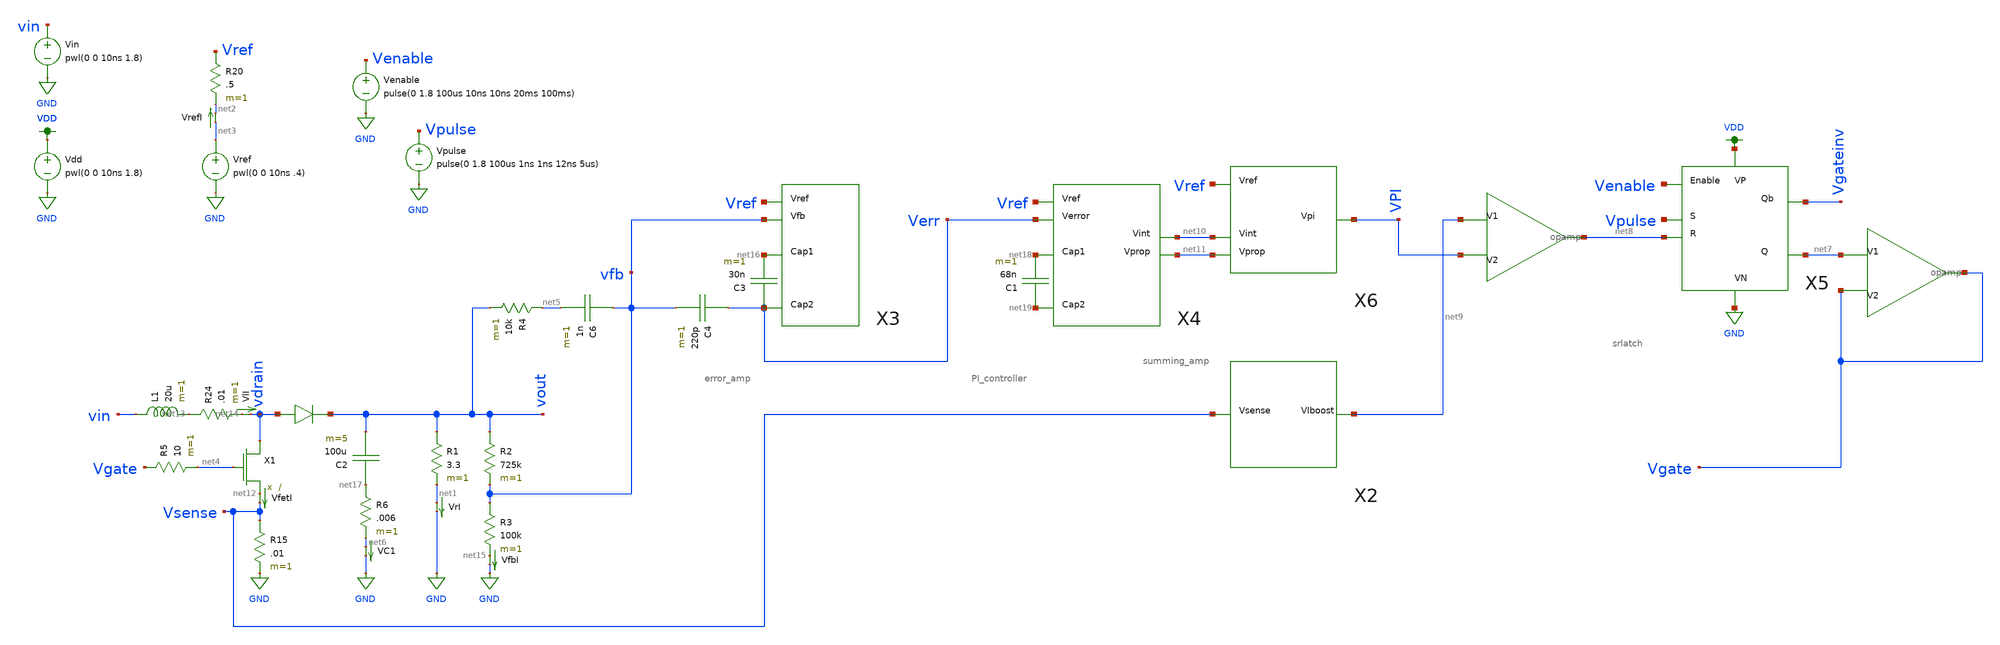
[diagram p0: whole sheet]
** sch_path: schematics/old/boost_CMC_tmp.sch
**.subckt boost_CMC_tmp
Vin vin GND pwl(0 0 10ns 1.8)
VfetI net12 Vsense 0
.save i(vfeti)
X1 vdrain net4 net12 power_nfet
L1 vin net13 20u m=1
D1 vdrain vout diode_schottky
R1 vout net1 3.3 m=1
VlI net14 vdrain 0
.save i(vli)
VrI net1 GND 0
.save i(vri)
R2 vout vfb 725k m=1
R3 vfb net15 100k m=1
Vdd VDD GND pwl(0 0 10ns 1.8)
Vref net3 GND pwl(0 0 10ns .4)
X11 net9 VPI net8 opamp
Vpulse Vpulse GND pulse(0 1.8 100us 1ns 1ns 12ns 5us)
VrefI net3 net2 0
.save i(vrefi)
R24 net13 net14 .01 m=1
VfbI net15 GND 0
.save i(vfbi)
R20 Vref net2 .5 m=1
C3 Verr net16 30n m=1
C4 Verr vfb 220p m=1
R4 net5 vout 10k m=1
C6 vfb net5 1n m=1
R5 Vgate net4 10 m=1
C2 net17 vout 100u m=5
R6 net17 net6 .006 m=1
VC1 net6 GND 0
.save i(vc1)
R15 Vsense GND .01 m=1
X5 Venable Vpulse net8 VDD GND Vgateinv net7 srlatch
X10 net7 Vgate Vgate opamp
Venable Venable GND pulse(0 1.8 100us 10ns 10ns 20ms 100ms)
X2 Vsense net9 current_boost
X3 Vref net16 vfb Verr error_amp
X4 Vref net18 Verr net19 net10 net11 PI_controller
C1 net19 net18 68n m=1
X6 Vref VPI net10 net11 summing_amp
**** begin user architecture code


.include ~/Documents/MADVLSI_final/schematics/models/power_nfet_model.spice
.include ~/Documents/MADVLSI_final/schematics/models/diode_schottky_model.spice
.options gmin=1e-10
.options abstol=1e-10
.options reltol=.003
.tran 100ns 10ms
.save v(vout)


.option wnflag=1
.lib ~/skywater/skywater-pdk/libraries/sky130_fd_pr_ngspice/latest/models/sky130.lib.spice tt

**** end user architecture code
**.ends

* expanding   symbol:  /home/madvlsi/Documents/MADVLSI_final/schematics/opamp.sym # of pins=3
** sym_path: schematics/opamp.sym
** sch_path: schematics/opamp.sch
.subckt opamp V1 V2 VOUT
*.ipin V1
*.ipin V2
*.opin VOUT
XM19 net12 net10 GND VDD sky130_fd_pr__pfet_01v8 L=.6 W=1.5 nf=1 ad='int((nf+1)/2) * W/nf * 0.29' as='int((nf+2)/2) * W/nf * 0.29'
+ pd='2*int((nf+1)/2) * (W/nf + 0.29)' ps='2*int((nf+2)/2) * (W/nf + 0.29)' nrd='0.29 / W' nrs='0.29 / W'
+ sa=0 sb=0 sd=0 mult=1 m=1
XMD20 VDD VDD net12 VDD sky130_fd_pr__pfet_01v8 L=.6 W=1.5 nf=1 ad='int((nf+1)/2) * W/nf * 0.29' as='int((nf+2)/2) * W/nf * 0.29'
+ pd='2*int((nf+1)/2) * (W/nf + 0.29)' ps='2*int((nf+2)/2) * (W/nf + 0.29)' nrd='0.29 / W' nrs='0.29 / W'
+ sa=0 sb=0 sd=0 mult=1 m=1
XM22 net12 net10 net9 VDD sky130_fd_pr__pfet_01v8 L=.6 W=1.5 nf=1 ad='int((nf+1)/2) * W/nf * 0.29' as='int((nf+2)/2) * W/nf * 0.29'
+ pd='2*int((nf+1)/2) * (W/nf + 0.29)' ps='2*int((nf+2)/2) * (W/nf + 0.29)' nrd='0.29 / W' nrs='0.29 / W'
+ sa=0 sb=0 sd=0 mult=1 m=1
XM23 GND net10 net12 VDD sky130_fd_pr__pfet_01v8 L=.6 W=1.5 nf=1 ad='int((nf+1)/2) * W/nf * 0.29' as='int((nf+2)/2) * W/nf * 0.29'
+ pd='2*int((nf+1)/2) * (W/nf + 0.29)' ps='2*int((nf+2)/2) * (W/nf + 0.29)' nrd='0.29 / W' nrs='0.29 / W'
+ sa=0 sb=0 sd=0 mult=1 m=1
XMD24 net9 VDD net10 VDD sky130_fd_pr__pfet_01v8 L=.6 W=1.5 nf=1 ad='int((nf+1)/2) * W/nf * 0.29' as='int((nf+2)/2) * W/nf * 0.29'
+ pd='2*int((nf+1)/2) * (W/nf + 0.29)' ps='2*int((nf+2)/2) * (W/nf + 0.29)' nrd='0.29 / W' nrs='0.29 / W'
+ sa=0 sb=0 sd=0 mult=1 m=1
XM25 VDD net10 net12 VDD sky130_fd_pr__pfet_01v8 L=.6 W=1.5 nf=1 ad='int((nf+1)/2) * W/nf * 0.29' as='int((nf+2)/2) * W/nf * 0.29'
+ pd='2*int((nf+1)/2) * (W/nf + 0.29)' ps='2*int((nf+2)/2) * (W/nf + 0.29)' nrd='0.29 / W' nrs='0.29 / W'
+ sa=0 sb=0 sd=0 mult=1 m=1
XM26 net7 V2 net11 VDD sky130_fd_pr__pfet_01v8 L=.6 W=1.5 nf=1 ad='int((nf+1)/2) * W/nf * 0.29' as='int((nf+2)/2) * W/nf * 0.29'
+ pd='2*int((nf+1)/2) * (W/nf + 0.29)' ps='2*int((nf+2)/2) * (W/nf + 0.29)' nrd='0.29 / W' nrs='0.29 / W'
+ sa=0 sb=0 sd=0 mult=1 m=1
XMD27 net5 VDD net14 VDD sky130_fd_pr__pfet_01v8 L=.6 W=1.5 nf=1 ad='int((nf+1)/2) * W/nf * 0.29' as='int((nf+2)/2) * W/nf * 0.29'
+ pd='2*int((nf+1)/2) * (W/nf + 0.29)' ps='2*int((nf+2)/2) * (W/nf + 0.29)' nrd='0.29 / W' nrs='0.29 / W'
+ sa=0 sb=0 sd=0 mult=1 m=1
XM28 net6 V1 net11 VDD sky130_fd_pr__pfet_01v8 L=.6 W=1.5 nf=1 ad='int((nf+1)/2) * W/nf * 0.29' as='int((nf+2)/2) * W/nf * 0.29'
+ pd='2*int((nf+1)/2) * (W/nf + 0.29)' ps='2*int((nf+2)/2) * (W/nf + 0.29)' nrd='0.29 / W' nrs='0.29 / W'
+ sa=0 sb=0 sd=0 mult=1 m=1
XM29 net11 net10 VDD VDD sky130_fd_pr__pfet_01v8 L=.6 W=1.5 nf=1 ad='int((nf+1)/2) * W/nf * 0.29' as='int((nf+2)/2) * W/nf * 0.29'
+ pd='2*int((nf+1)/2) * (W/nf + 0.29)' ps='2*int((nf+2)/2) * (W/nf + 0.29)' nrd='0.29 / W' nrs='0.29 / W'
+ sa=0 sb=0 sd=0 mult=1 m=1
XMD30 net11 VDD VDD VDD sky130_fd_pr__pfet_01v8 L=.6 W=1.5 nf=1 ad='int((nf+1)/2) * W/nf * 0.29' as='int((nf+2)/2) * W/nf * 0.29'
+ pd='2*int((nf+1)/2) * (W/nf + 0.29)' ps='2*int((nf+2)/2) * (W/nf + 0.29)' nrd='0.29 / W' nrs='0.29 / W'
+ sa=0 sb=0 sd=0 mult=1 m=1
XMD31 net2 VDD net13 VDD sky130_fd_pr__pfet_01v8 L=.6 W=1.5 nf=1 ad='int((nf+1)/2) * W/nf * 0.29' as='int((nf+2)/2) * W/nf * 0.29'
+ pd='2*int((nf+1)/2) * (W/nf + 0.29)' ps='2*int((nf+2)/2) * (W/nf + 0.29)' nrd='0.29 / W' nrs='0.29 / W'
+ sa=0 sb=0 sd=0 mult=1 m=1
XM32 net4 net5 net5 VDD sky130_fd_pr__pfet_01v8 L=.6 W=1.5 nf=1 ad='int((nf+1)/2) * W/nf * 0.29' as='int((nf+2)/2) * W/nf * 0.29'
+ pd='2*int((nf+1)/2) * (W/nf + 0.29)' ps='2*int((nf+2)/2) * (W/nf + 0.29)' nrd='0.29 / W' nrs='0.29 / W'
+ sa=0 sb=0 sd=0 mult=1 m=1
XM33 VDD net10 net4 VDD sky130_fd_pr__pfet_01v8 L=.6 W=1.5 nf=1 ad='int((nf+1)/2) * W/nf * 0.29' as='int((nf+2)/2) * W/nf * 0.29'
+ pd='2*int((nf+1)/2) * (W/nf + 0.29)' ps='2*int((nf+2)/2) * (W/nf + 0.29)' nrd='0.29 / W' nrs='0.29 / W'
+ sa=0 sb=0 sd=0 mult=1 m=1
XM34 net3 net5 net2 VDD sky130_fd_pr__pfet_01v8 L=.6 W=1.5 nf=1 ad='int((nf+1)/2) * W/nf * 0.29' as='int((nf+2)/2) * W/nf * 0.29'
+ pd='2*int((nf+1)/2) * (W/nf + 0.29)' ps='2*int((nf+2)/2) * (W/nf + 0.29)' nrd='0.29 / W' nrs='0.29 / W'
+ sa=0 sb=0 sd=0 mult=1 m=1
XM35 VDD net10 net3 VDD sky130_fd_pr__pfet_01v8 L=.6 W=1.5 nf=1 ad='int((nf+1)/2) * W/nf * 0.29' as='int((nf+2)/2) * W/nf * 0.29'
+ pd='2*int((nf+1)/2) * (W/nf + 0.29)' ps='2*int((nf+2)/2) * (W/nf + 0.29)' nrd='0.29 / W' nrs='0.29 / W'
+ sa=0 sb=0 sd=0 mult=1 m=1
XM36 VOUT net2 VDD VDD sky130_fd_pr__pfet_01v8 L=.6 W=1.5 nf=1 ad='int((nf+1)/2) * W/nf * 0.29' as='int((nf+2)/2) * W/nf * 0.29'
+ pd='2*int((nf+1)/2) * (W/nf + 0.29)' ps='2*int((nf+2)/2) * (W/nf + 0.29)' nrd='0.29 / W' nrs='0.29 / W'
+ sa=0 sb=0 sd=0 mult=1 m=1
XM37 VDD net2 VOUT VDD sky130_fd_pr__pfet_01v8 L=.6 W=1.5 nf=1 ad='int((nf+1)/2) * W/nf * 0.29' as='int((nf+2)/2) * W/nf * 0.29'
+ pd='2*int((nf+1)/2) * (W/nf + 0.29)' ps='2*int((nf+2)/2) * (W/nf + 0.29)' nrd='0.29 / W' nrs='0.29 / W'
+ sa=0 sb=0 sd=0 mult=1 m=1
XM38 VOUT net2 VDD VDD sky130_fd_pr__pfet_01v8 L=.6 W=1.5 nf=1 ad='int((nf+1)/2) * W/nf * 0.29' as='int((nf+2)/2) * W/nf * 0.29'
+ pd='2*int((nf+1)/2) * (W/nf + 0.29)' ps='2*int((nf+2)/2) * (W/nf + 0.29)' nrd='0.29 / W' nrs='0.29 / W'
+ sa=0 sb=0 sd=0 mult=1 m=1
XM39 VDD net2 VOUT VDD sky130_fd_pr__pfet_01v8 L=.6 W=1.5 nf=1 ad='int((nf+1)/2) * W/nf * 0.29' as='int((nf+2)/2) * W/nf * 0.29'
+ pd='2*int((nf+1)/2) * (W/nf + 0.29)' ps='2*int((nf+2)/2) * (W/nf + 0.29)' nrd='0.29 / W' nrs='0.29 / W'
+ sa=0 sb=0 sd=0 mult=1 m=1
XM40 net1 net9 VDD GND sky130_fd_pr__nfet_01v8 L=.6 W=1.5 nf=1 ad='int((nf+1)/2) * W/nf * 0.29' as='int((nf+2)/2) * W/nf * 0.29'
+ pd='2*int((nf+1)/2) * (W/nf + 0.29)' ps='2*int((nf+2)/2) * (W/nf + 0.29)' nrd='0.29 / W' nrs='0.29 / W'
+ sa=0 sb=0 sd=0 mult=1 m=1
XMD41 GND GND net1 GND sky130_fd_pr__nfet_01v8 L=.6 W=1.5 nf=1 ad='int((nf+1)/2) * W/nf * 0.29' as='int((nf+2)/2) * W/nf * 0.29'
+ pd='2*int((nf+1)/2) * (W/nf + 0.29)' ps='2*int((nf+2)/2) * (W/nf + 0.29)' nrd='0.29 / W' nrs='0.29 / W'
+ sa=0 sb=0 sd=0 mult=1 m=1
XM42 net1 net9 net10 GND sky130_fd_pr__nfet_01v8 L=.6 W=1.5 nf=1 ad='int((nf+1)/2) * W/nf * 0.29' as='int((nf+2)/2) * W/nf * 0.29'
+ pd='2*int((nf+1)/2) * (W/nf + 0.29)' ps='2*int((nf+2)/2) * (W/nf + 0.29)' nrd='0.29 / W' nrs='0.29 / W'
+ sa=0 sb=0 sd=0 mult=1 m=1
XM43 VDD net9 net1 GND sky130_fd_pr__nfet_01v8 L=.6 W=1.5 nf=1 ad='int((nf+1)/2) * W/nf * 0.29' as='int((nf+2)/2) * W/nf * 0.29'
+ pd='2*int((nf+1)/2) * (W/nf + 0.29)' ps='2*int((nf+2)/2) * (W/nf + 0.29)' nrd='0.29 / W' nrs='0.29 / W'
+ sa=0 sb=0 sd=0 mult=1 m=1
XMD44 net10 GND net9 GND sky130_fd_pr__nfet_01v8 L=.6 W=1.5 nf=1 ad='int((nf+1)/2) * W/nf * 0.29' as='int((nf+2)/2) * W/nf * 0.29'
+ pd='2*int((nf+1)/2) * (W/nf + 0.29)' ps='2*int((nf+2)/2) * (W/nf + 0.29)' nrd='0.29 / W' nrs='0.29 / W'
+ sa=0 sb=0 sd=0 mult=1 m=1
XM45 GND net9 net1 GND sky130_fd_pr__nfet_01v8 L=.6 W=1.5 nf=1 ad='int((nf+1)/2) * W/nf * 0.29' as='int((nf+2)/2) * W/nf * 0.29'
+ pd='2*int((nf+1)/2) * (W/nf + 0.29)' ps='2*int((nf+2)/2) * (W/nf + 0.29)' nrd='0.29 / W' nrs='0.29 / W'
+ sa=0 sb=0 sd=0 mult=1 m=1
XM46 net3 V1 net8 GND sky130_fd_pr__nfet_01v8 L=.6 W=1.5 nf=1 ad='int((nf+1)/2) * W/nf * 0.29' as='int((nf+2)/2) * W/nf * 0.29'
+ pd='2*int((nf+1)/2) * (W/nf + 0.29)' ps='2*int((nf+2)/2) * (W/nf + 0.29)' nrd='0.29 / W' nrs='0.29 / W'
+ sa=0 sb=0 sd=0 mult=1 m=1
XMD47 net5 GND net15 GND sky130_fd_pr__nfet_01v8 L=.6 W=1.5 nf=1 ad='int((nf+1)/2) * W/nf * 0.29' as='int((nf+2)/2) * W/nf * 0.29'
+ pd='2*int((nf+1)/2) * (W/nf + 0.29)' ps='2*int((nf+2)/2) * (W/nf + 0.29)' nrd='0.29 / W' nrs='0.29 / W'
+ sa=0 sb=0 sd=0 mult=1 m=1
XM48 net4 V2 net8 GND sky130_fd_pr__nfet_01v8 L=.6 W=1.5 nf=1 ad='int((nf+1)/2) * W/nf * 0.29' as='int((nf+2)/2) * W/nf * 0.29'
+ pd='2*int((nf+1)/2) * (W/nf + 0.29)' ps='2*int((nf+2)/2) * (W/nf + 0.29)' nrd='0.29 / W' nrs='0.29 / W'
+ sa=0 sb=0 sd=0 mult=1 m=1
XM49 net8 net9 GND GND sky130_fd_pr__nfet_01v8 L=.6 W=1.5 nf=1 ad='int((nf+1)/2) * W/nf * 0.29' as='int((nf+2)/2) * W/nf * 0.29'
+ pd='2*int((nf+1)/2) * (W/nf + 0.29)' ps='2*int((nf+2)/2) * (W/nf + 0.29)' nrd='0.29 / W' nrs='0.29 / W'
+ sa=0 sb=0 sd=0 mult=1 m=1
XMD50 net8 GND GND GND sky130_fd_pr__nfet_01v8 L=.6 W=1.5 nf=1 ad='int((nf+1)/2) * W/nf * 0.29' as='int((nf+2)/2) * W/nf * 0.29'
+ pd='2*int((nf+1)/2) * (W/nf + 0.29)' ps='2*int((nf+2)/2) * (W/nf + 0.29)' nrd='0.29 / W' nrs='0.29 / W'
+ sa=0 sb=0 sd=0 mult=1 m=1
XMD51 net2 GND net16 GND sky130_fd_pr__nfet_01v8 L=.6 W=1.5 nf=1 ad='int((nf+1)/2) * W/nf * 0.29' as='int((nf+2)/2) * W/nf * 0.29'
+ pd='2*int((nf+1)/2) * (W/nf + 0.29)' ps='2*int((nf+2)/2) * (W/nf + 0.29)' nrd='0.29 / W' nrs='0.29 / W'
+ sa=0 sb=0 sd=0 mult=1 m=1
XM52 GND net9 net7 GND sky130_fd_pr__nfet_01v8 L=.6 W=1.5 nf=1 ad='int((nf+1)/2) * W/nf * 0.29' as='int((nf+2)/2) * W/nf * 0.29'
+ pd='2*int((nf+1)/2) * (W/nf + 0.29)' ps='2*int((nf+2)/2) * (W/nf + 0.29)' nrd='0.29 / W' nrs='0.29 / W'
+ sa=0 sb=0 sd=0 mult=1 m=1
XMD53 VOUT GND GND GND sky130_fd_pr__nfet_01v8 L=.6 W=1.5 nf=1 ad='int((nf+1)/2) * W/nf * 0.29' as='int((nf+2)/2) * W/nf * 0.29'
+ pd='2*int((nf+1)/2) * (W/nf + 0.29)' ps='2*int((nf+2)/2) * (W/nf + 0.29)' nrd='0.29 / W' nrs='0.29 / W'
+ sa=0 sb=0 sd=0 mult=1 m=1
XM54 GND net9 net6 GND sky130_fd_pr__nfet_01v8 L=.6 W=1.5 nf=1 ad='int((nf+1)/2) * W/nf * 0.29' as='int((nf+2)/2) * W/nf * 0.29'
+ pd='2*int((nf+1)/2) * (W/nf + 0.29)' ps='2*int((nf+2)/2) * (W/nf + 0.29)' nrd='0.29 / W' nrs='0.29 / W'
+ sa=0 sb=0 sd=0 mult=1 m=1
XM55 net7 net5 net5 GND sky130_fd_pr__nfet_01v8 L=.6 W=1.5 nf=1 ad='int((nf+1)/2) * W/nf * 0.29' as='int((nf+2)/2) * W/nf * 0.29'
+ pd='2*int((nf+1)/2) * (W/nf + 0.29)' ps='2*int((nf+2)/2) * (W/nf + 0.29)' nrd='0.29 / W' nrs='0.29 / W'
+ sa=0 sb=0 sd=0 mult=1 m=1
XM56 net6 net5 net2 GND sky130_fd_pr__nfet_01v8 L=.6 W=1.5 nf=1 ad='int((nf+1)/2) * W/nf * 0.29' as='int((nf+2)/2) * W/nf * 0.29'
+ pd='2*int((nf+1)/2) * (W/nf + 0.29)' ps='2*int((nf+2)/2) * (W/nf + 0.29)' nrd='0.29 / W' nrs='0.29 / W'
+ sa=0 sb=0 sd=0 mult=1 m=1
XMD57 VOUT GND GND GND sky130_fd_pr__nfet_01v8 L=.6 W=1.5 nf=1 ad='int((nf+1)/2) * W/nf * 0.29' as='int((nf+2)/2) * W/nf * 0.29'
+ pd='2*int((nf+1)/2) * (W/nf + 0.29)' ps='2*int((nf+2)/2) * (W/nf + 0.29)' nrd='0.29 / W' nrs='0.29 / W'
+ sa=0 sb=0 sd=0 mult=1 m=1
XM58 GND net2 VOUT GND sky130_fd_pr__nfet_01v8 L=.6 W=1.5 nf=1 ad='int((nf+1)/2) * W/nf * 0.29' as='int((nf+2)/2) * W/nf * 0.29'
+ pd='2*int((nf+1)/2) * (W/nf + 0.29)' ps='2*int((nf+2)/2) * (W/nf + 0.29)' nrd='0.29 / W' nrs='0.29 / W'
+ sa=0 sb=0 sd=0 mult=1 m=1
XM59 GND net2 VOUT GND sky130_fd_pr__nfet_01v8 L=.6 W=1.5 nf=1 ad='int((nf+1)/2) * W/nf * 0.29' as='int((nf+2)/2) * W/nf * 0.29'
+ pd='2*int((nf+1)/2) * (W/nf + 0.29)' ps='2*int((nf+2)/2) * (W/nf + 0.29)' nrd='0.29 / W' nrs='0.29 / W'
+ sa=0 sb=0 sd=0 mult=1 m=1
XM60 net12 net10 GND VDD sky130_fd_pr__pfet_01v8 L=.6 W=1.5 nf=1 ad='int((nf+1)/2) * W/nf * 0.29' as='int((nf+2)/2) * W/nf * 0.29'
+ pd='2*int((nf+1)/2) * (W/nf + 0.29)' ps='2*int((nf+2)/2) * (W/nf + 0.29)' nrd='0.29 / W' nrs='0.29 / W'
+ sa=0 sb=0 sd=0 mult=1 m=1
XM61 net10 net10 net4 VDD sky130_fd_pr__pfet_01v8 L=.6 W=1.5 nf=1 ad='int((nf+1)/2) * W/nf * 0.29' as='int((nf+2)/2) * W/nf * 0.29'
+ pd='2*int((nf+1)/2) * (W/nf + 0.29)' ps='2*int((nf+2)/2) * (W/nf + 0.29)' nrd='0.29 / W' nrs='0.29 / W'
+ sa=0 sb=0 sd=0 mult=1 m=1
XM62 net1 net9 VDD GND sky130_fd_pr__nfet_01v8 L=.6 W=1.5 nf=1 ad='int((nf+1)/2) * W/nf * 0.29' as='int((nf+2)/2) * W/nf * 0.29'
+ pd='2*int((nf+1)/2) * (W/nf + 0.29)' ps='2*int((nf+2)/2) * (W/nf + 0.29)' nrd='0.29 / W' nrs='0.29 / W'
+ sa=0 sb=0 sd=0 mult=1 m=1
XM63 net9 net9 net7 GND sky130_fd_pr__nfet_01v8 L=.6 W=1.5 nf=1 ad='int((nf+1)/2) * W/nf * 0.29' as='int((nf+2)/2) * W/nf * 0.29'
+ pd='2*int((nf+1)/2) * (W/nf + 0.29)' ps='2*int((nf+2)/2) * (W/nf + 0.29)' nrd='0.29 / W' nrs='0.29 / W'
+ sa=0 sb=0 sd=0 mult=1 m=1
XMD64 VDD GND GND GND sky130_fd_pr__nfet_01v8 L=.6 W=1.5 nf=1 ad='int((nf+1)/2) * W/nf * 0.29' as='int((nf+2)/2) * W/nf * 0.29'
+ pd='2*int((nf+1)/2) * (W/nf + 0.29)' ps='2*int((nf+2)/2) * (W/nf + 0.29)' nrd='0.29 / W' nrs='0.29 / W'
+ sa=0 sb=0 sd=0 mult=1 m=1
XMD65 net7 GND GND GND sky130_fd_pr__nfet_01v8 L=.6 W=1.5 nf=1 ad='int((nf+1)/2) * W/nf * 0.29' as='int((nf+2)/2) * W/nf * 0.29'
+ pd='2*int((nf+1)/2) * (W/nf + 0.29)' ps='2*int((nf+2)/2) * (W/nf + 0.29)' nrd='0.29 / W' nrs='0.29 / W'
+ sa=0 sb=0 sd=0 mult=1 m=1
XMD66 GND VDD VDD VDD sky130_fd_pr__pfet_01v8 L=.6 W=1.5 nf=1 ad='int((nf+1)/2) * W/nf * 0.29' as='int((nf+2)/2) * W/nf * 0.29'
+ pd='2*int((nf+1)/2) * (W/nf + 0.29)' ps='2*int((nf+2)/2) * (W/nf + 0.29)' nrd='0.29 / W' nrs='0.29 / W'
+ sa=0 sb=0 sd=0 mult=1 m=1
XMD67 net4 VDD VDD VDD sky130_fd_pr__pfet_01v8 L=.6 W=1.5 nf=1 ad='int((nf+1)/2) * W/nf * 0.29' as='int((nf+2)/2) * W/nf * 0.29'
+ pd='2*int((nf+1)/2) * (W/nf + 0.29)' ps='2*int((nf+2)/2) * (W/nf + 0.29)' nrd='0.29 / W' nrs='0.29 / W'
+ sa=0 sb=0 sd=0 mult=1 m=1
XMD1 net15 GND net3 GND sky130_fd_pr__nfet_01v8 L=.6 W=1.5 nf=1 ad='int((nf+1)/2) * W/nf * 0.29' as='int((nf+2)/2) * W/nf * 0.29'
+ pd='2*int((nf+1)/2) * (W/nf + 0.29)' ps='2*int((nf+2)/2) * (W/nf + 0.29)' nrd='0.29 / W' nrs='0.29 / W'
+ sa=0 sb=0 sd=0 mult=1 m=1
XMD2 net16 GND net4 GND sky130_fd_pr__nfet_01v8 L=.6 W=1.5 nf=1 ad='int((nf+1)/2) * W/nf * 0.29' as='int((nf+2)/2) * W/nf * 0.29'
+ pd='2*int((nf+1)/2) * (W/nf + 0.29)' ps='2*int((nf+2)/2) * (W/nf + 0.29)' nrd='0.29 / W' nrs='0.29 / W'
+ sa=0 sb=0 sd=0 mult=1 m=1
XMD3 net13 VDD net6 VDD sky130_fd_pr__pfet_01v8 L=.6 W=1.5 nf=1 ad='int((nf+1)/2) * W/nf * 0.29' as='int((nf+2)/2) * W/nf * 0.29'
+ pd='2*int((nf+1)/2) * (W/nf + 0.29)' ps='2*int((nf+2)/2) * (W/nf + 0.29)' nrd='0.29 / W' nrs='0.29 / W'
+ sa=0 sb=0 sd=0 mult=1 m=1
XMD4 net14 VDD net7 VDD sky130_fd_pr__pfet_01v8 L=.6 W=1.5 nf=1 ad='int((nf+1)/2) * W/nf * 0.29' as='int((nf+2)/2) * W/nf * 0.29'
+ pd='2*int((nf+1)/2) * (W/nf + 0.29)' ps='2*int((nf+2)/2) * (W/nf + 0.29)' nrd='0.29 / W' nrs='0.29 / W'
+ sa=0 sb=0 sd=0 mult=1 m=1
XM1 net21 net10 GND VDD sky130_fd_pr__pfet_01v8 L=.6 W=1.5 nf=1 ad='int((nf+1)/2) * W/nf * 0.29' as='int((nf+2)/2) * W/nf * 0.29'
+ pd='2*int((nf+1)/2) * (W/nf + 0.29)' ps='2*int((nf+2)/2) * (W/nf + 0.29)' nrd='0.29 / W' nrs='0.29 / W'
+ sa=0 sb=0 sd=0 mult=1 m=1
XMD5 VDD VDD net21 VDD sky130_fd_pr__pfet_01v8 L=.6 W=1.5 nf=1 ad='int((nf+1)/2) * W/nf * 0.29' as='int((nf+2)/2) * W/nf * 0.29'
+ pd='2*int((nf+1)/2) * (W/nf + 0.29)' ps='2*int((nf+2)/2) * (W/nf + 0.29)' nrd='0.29 / W' nrs='0.29 / W'
+ sa=0 sb=0 sd=0 mult=1 m=1
XM6 net21 net10 net9 VDD sky130_fd_pr__pfet_01v8 L=.6 W=1.5 nf=1 ad='int((nf+1)/2) * W/nf * 0.29' as='int((nf+2)/2) * W/nf * 0.29'
+ pd='2*int((nf+1)/2) * (W/nf + 0.29)' ps='2*int((nf+2)/2) * (W/nf + 0.29)' nrd='0.29 / W' nrs='0.29 / W'
+ sa=0 sb=0 sd=0 mult=1 m=1
XM7 GND net10 net21 VDD sky130_fd_pr__pfet_01v8 L=.6 W=1.5 nf=1 ad='int((nf+1)/2) * W/nf * 0.29' as='int((nf+2)/2) * W/nf * 0.29'
+ pd='2*int((nf+1)/2) * (W/nf + 0.29)' ps='2*int((nf+2)/2) * (W/nf + 0.29)' nrd='0.29 / W' nrs='0.29 / W'
+ sa=0 sb=0 sd=0 mult=1 m=1
XMD8 net9 VDD net10 VDD sky130_fd_pr__pfet_01v8 L=.6 W=1.5 nf=1 ad='int((nf+1)/2) * W/nf * 0.29' as='int((nf+2)/2) * W/nf * 0.29'
+ pd='2*int((nf+1)/2) * (W/nf + 0.29)' ps='2*int((nf+2)/2) * (W/nf + 0.29)' nrd='0.29 / W' nrs='0.29 / W'
+ sa=0 sb=0 sd=0 mult=1 m=1
XM9 VDD net10 net21 VDD sky130_fd_pr__pfet_01v8 L=.6 W=1.5 nf=1 ad='int((nf+1)/2) * W/nf * 0.29' as='int((nf+2)/2) * W/nf * 0.29'
+ pd='2*int((nf+1)/2) * (W/nf + 0.29)' ps='2*int((nf+2)/2) * (W/nf + 0.29)' nrd='0.29 / W' nrs='0.29 / W'
+ sa=0 sb=0 sd=0 mult=1 m=1
XM10 net7 V2 net20 VDD sky130_fd_pr__pfet_01v8 L=.6 W=1.5 nf=1 ad='int((nf+1)/2) * W/nf * 0.29' as='int((nf+2)/2) * W/nf * 0.29'
+ pd='2*int((nf+1)/2) * (W/nf + 0.29)' ps='2*int((nf+2)/2) * (W/nf + 0.29)' nrd='0.29 / W' nrs='0.29 / W'
+ sa=0 sb=0 sd=0 mult=1 m=1
XMD11 net18 VDD net23 VDD sky130_fd_pr__pfet_01v8 L=.6 W=1.5 nf=1 ad='int((nf+1)/2) * W/nf * 0.29' as='int((nf+2)/2) * W/nf * 0.29'
+ pd='2*int((nf+1)/2) * (W/nf + 0.29)' ps='2*int((nf+2)/2) * (W/nf + 0.29)' nrd='0.29 / W' nrs='0.29 / W'
+ sa=0 sb=0 sd=0 mult=1 m=1
XM12 net6 V1 net20 VDD sky130_fd_pr__pfet_01v8 L=.6 W=1.5 nf=1 ad='int((nf+1)/2) * W/nf * 0.29' as='int((nf+2)/2) * W/nf * 0.29'
+ pd='2*int((nf+1)/2) * (W/nf + 0.29)' ps='2*int((nf+2)/2) * (W/nf + 0.29)' nrd='0.29 / W' nrs='0.29 / W'
+ sa=0 sb=0 sd=0 mult=1 m=1
XM13 net20 net10 VDD VDD sky130_fd_pr__pfet_01v8 L=.6 W=1.5 nf=1 ad='int((nf+1)/2) * W/nf * 0.29' as='int((nf+2)/2) * W/nf * 0.29'
+ pd='2*int((nf+1)/2) * (W/nf + 0.29)' ps='2*int((nf+2)/2) * (W/nf + 0.29)' nrd='0.29 / W' nrs='0.29 / W'
+ sa=0 sb=0 sd=0 mult=1 m=1
XMD14 net20 VDD VDD VDD sky130_fd_pr__pfet_01v8 L=.6 W=1.5 nf=1 ad='int((nf+1)/2) * W/nf * 0.29' as='int((nf+2)/2) * W/nf * 0.29'
+ pd='2*int((nf+1)/2) * (W/nf + 0.29)' ps='2*int((nf+2)/2) * (W/nf + 0.29)' nrd='0.29 / W' nrs='0.29 / W'
+ sa=0 sb=0 sd=0 mult=1 m=1
XMD15 net2 VDD net22 VDD sky130_fd_pr__pfet_01v8 L=.6 W=1.5 nf=1 ad='int((nf+1)/2) * W/nf * 0.29' as='int((nf+2)/2) * W/nf * 0.29'
+ pd='2*int((nf+1)/2) * (W/nf + 0.29)' ps='2*int((nf+2)/2) * (W/nf + 0.29)' nrd='0.29 / W' nrs='0.29 / W'
+ sa=0 sb=0 sd=0 mult=1 m=1
XM16 net4 net18 net18 VDD sky130_fd_pr__pfet_01v8 L=.6 W=1.5 nf=1 ad='int((nf+1)/2) * W/nf * 0.29' as='int((nf+2)/2) * W/nf * 0.29'
+ pd='2*int((nf+1)/2) * (W/nf + 0.29)' ps='2*int((nf+2)/2) * (W/nf + 0.29)' nrd='0.29 / W' nrs='0.29 / W'
+ sa=0 sb=0 sd=0 mult=1 m=1
XM17 VDD net10 net4 VDD sky130_fd_pr__pfet_01v8 L=.6 W=1.5 nf=1 ad='int((nf+1)/2) * W/nf * 0.29' as='int((nf+2)/2) * W/nf * 0.29'
+ pd='2*int((nf+1)/2) * (W/nf + 0.29)' ps='2*int((nf+2)/2) * (W/nf + 0.29)' nrd='0.29 / W' nrs='0.29 / W'
+ sa=0 sb=0 sd=0 mult=1 m=1
XM18 net3 net18 net2 VDD sky130_fd_pr__pfet_01v8 L=.6 W=1.5 nf=1 ad='int((nf+1)/2) * W/nf * 0.29' as='int((nf+2)/2) * W/nf * 0.29'
+ pd='2*int((nf+1)/2) * (W/nf + 0.29)' ps='2*int((nf+2)/2) * (W/nf + 0.29)' nrd='0.29 / W' nrs='0.29 / W'
+ sa=0 sb=0 sd=0 mult=1 m=1
XM20 VDD net10 net3 VDD sky130_fd_pr__pfet_01v8 L=.6 W=1.5 nf=1 ad='int((nf+1)/2) * W/nf * 0.29' as='int((nf+2)/2) * W/nf * 0.29'
+ pd='2*int((nf+1)/2) * (W/nf + 0.29)' ps='2*int((nf+2)/2) * (W/nf + 0.29)' nrd='0.29 / W' nrs='0.29 / W'
+ sa=0 sb=0 sd=0 mult=1 m=1
XM21 VOUT net2 VDD VDD sky130_fd_pr__pfet_01v8 L=.6 W=1.5 nf=1 ad='int((nf+1)/2) * W/nf * 0.29' as='int((nf+2)/2) * W/nf * 0.29'
+ pd='2*int((nf+1)/2) * (W/nf + 0.29)' ps='2*int((nf+2)/2) * (W/nf + 0.29)' nrd='0.29 / W' nrs='0.29 / W'
+ sa=0 sb=0 sd=0 mult=1 m=1
XM24 VDD net2 VOUT VDD sky130_fd_pr__pfet_01v8 L=.6 W=1.5 nf=1 ad='int((nf+1)/2) * W/nf * 0.29' as='int((nf+2)/2) * W/nf * 0.29'
+ pd='2*int((nf+1)/2) * (W/nf + 0.29)' ps='2*int((nf+2)/2) * (W/nf + 0.29)' nrd='0.29 / W' nrs='0.29 / W'
+ sa=0 sb=0 sd=0 mult=1 m=1
XM27 VOUT net2 VDD VDD sky130_fd_pr__pfet_01v8 L=.6 W=1.5 nf=1 ad='int((nf+1)/2) * W/nf * 0.29' as='int((nf+2)/2) * W/nf * 0.29'
+ pd='2*int((nf+1)/2) * (W/nf + 0.29)' ps='2*int((nf+2)/2) * (W/nf + 0.29)' nrd='0.29 / W' nrs='0.29 / W'
+ sa=0 sb=0 sd=0 mult=1 m=1
XM30 VDD net2 VOUT VDD sky130_fd_pr__pfet_01v8 L=.6 W=1.5 nf=1 ad='int((nf+1)/2) * W/nf * 0.29' as='int((nf+2)/2) * W/nf * 0.29'
+ pd='2*int((nf+1)/2) * (W/nf + 0.29)' ps='2*int((nf+2)/2) * (W/nf + 0.29)' nrd='0.29 / W' nrs='0.29 / W'
+ sa=0 sb=0 sd=0 mult=1 m=1
XM31 net17 net9 VDD GND sky130_fd_pr__nfet_01v8 L=.6 W=1.5 nf=1 ad='int((nf+1)/2) * W/nf * 0.29' as='int((nf+2)/2) * W/nf * 0.29'
+ pd='2*int((nf+1)/2) * (W/nf + 0.29)' ps='2*int((nf+2)/2) * (W/nf + 0.29)' nrd='0.29 / W' nrs='0.29 / W'
+ sa=0 sb=0 sd=0 mult=1 m=1
XMD32 GND GND net17 GND sky130_fd_pr__nfet_01v8 L=.6 W=1.5 nf=1 ad='int((nf+1)/2) * W/nf * 0.29' as='int((nf+2)/2) * W/nf * 0.29'
+ pd='2*int((nf+1)/2) * (W/nf + 0.29)' ps='2*int((nf+2)/2) * (W/nf + 0.29)' nrd='0.29 / W' nrs='0.29 / W'
+ sa=0 sb=0 sd=0 mult=1 m=1
XM41 net17 net9 net10 GND sky130_fd_pr__nfet_01v8 L=.6 W=1.5 nf=1 ad='int((nf+1)/2) * W/nf * 0.29' as='int((nf+2)/2) * W/nf * 0.29'
+ pd='2*int((nf+1)/2) * (W/nf + 0.29)' ps='2*int((nf+2)/2) * (W/nf + 0.29)' nrd='0.29 / W' nrs='0.29 / W'
+ sa=0 sb=0 sd=0 mult=1 m=1
XM44 VDD net9 net17 GND sky130_fd_pr__nfet_01v8 L=.6 W=1.5 nf=1 ad='int((nf+1)/2) * W/nf * 0.29' as='int((nf+2)/2) * W/nf * 0.29'
+ pd='2*int((nf+1)/2) * (W/nf + 0.29)' ps='2*int((nf+2)/2) * (W/nf + 0.29)' nrd='0.29 / W' nrs='0.29 / W'
+ sa=0 sb=0 sd=0 mult=1 m=1
XMD45 net10 GND net9 GND sky130_fd_pr__nfet_01v8 L=.6 W=1.5 nf=1 ad='int((nf+1)/2) * W/nf * 0.29' as='int((nf+2)/2) * W/nf * 0.29'
+ pd='2*int((nf+1)/2) * (W/nf + 0.29)' ps='2*int((nf+2)/2) * (W/nf + 0.29)' nrd='0.29 / W' nrs='0.29 / W'
+ sa=0 sb=0 sd=0 mult=1 m=1
XM47 GND net9 net17 GND sky130_fd_pr__nfet_01v8 L=.6 W=1.5 nf=1 ad='int((nf+1)/2) * W/nf * 0.29' as='int((nf+2)/2) * W/nf * 0.29'
+ pd='2*int((nf+1)/2) * (W/nf + 0.29)' ps='2*int((nf+2)/2) * (W/nf + 0.29)' nrd='0.29 / W' nrs='0.29 / W'
+ sa=0 sb=0 sd=0 mult=1 m=1
XM50 net3 V1 net19 GND sky130_fd_pr__nfet_01v8 L=.6 W=1.5 nf=1 ad='int((nf+1)/2) * W/nf * 0.29' as='int((nf+2)/2) * W/nf * 0.29'
+ pd='2*int((nf+1)/2) * (W/nf + 0.29)' ps='2*int((nf+2)/2) * (W/nf + 0.29)' nrd='0.29 / W' nrs='0.29 / W'
+ sa=0 sb=0 sd=0 mult=1 m=1
XMD52 net18 GND net24 GND sky130_fd_pr__nfet_01v8 L=.6 W=1.5 nf=1 ad='int((nf+1)/2) * W/nf * 0.29' as='int((nf+2)/2) * W/nf * 0.29'
+ pd='2*int((nf+1)/2) * (W/nf + 0.29)' ps='2*int((nf+2)/2) * (W/nf + 0.29)' nrd='0.29 / W' nrs='0.29 / W'
+ sa=0 sb=0 sd=0 mult=1 m=1
XM53 net4 V2 net19 GND sky130_fd_pr__nfet_01v8 L=.6 W=1.5 nf=1 ad='int((nf+1)/2) * W/nf * 0.29' as='int((nf+2)/2) * W/nf * 0.29'
+ pd='2*int((nf+1)/2) * (W/nf + 0.29)' ps='2*int((nf+2)/2) * (W/nf + 0.29)' nrd='0.29 / W' nrs='0.29 / W'
+ sa=0 sb=0 sd=0 mult=1 m=1
XM57 net19 net9 GND GND sky130_fd_pr__nfet_01v8 L=.6 W=1.5 nf=1 ad='int((nf+1)/2) * W/nf * 0.29' as='int((nf+2)/2) * W/nf * 0.29'
+ pd='2*int((nf+1)/2) * (W/nf + 0.29)' ps='2*int((nf+2)/2) * (W/nf + 0.29)' nrd='0.29 / W' nrs='0.29 / W'
+ sa=0 sb=0 sd=0 mult=1 m=1
XMD58 net19 GND GND GND sky130_fd_pr__nfet_01v8 L=.6 W=1.5 nf=1 ad='int((nf+1)/2) * W/nf * 0.29' as='int((nf+2)/2) * W/nf * 0.29'
+ pd='2*int((nf+1)/2) * (W/nf + 0.29)' ps='2*int((nf+2)/2) * (W/nf + 0.29)' nrd='0.29 / W' nrs='0.29 / W'
+ sa=0 sb=0 sd=0 mult=1 m=1
XMD59 net2 GND net25 GND sky130_fd_pr__nfet_01v8 L=.6 W=1.5 nf=1 ad='int((nf+1)/2) * W/nf * 0.29' as='int((nf+2)/2) * W/nf * 0.29'
+ pd='2*int((nf+1)/2) * (W/nf + 0.29)' ps='2*int((nf+2)/2) * (W/nf + 0.29)' nrd='0.29 / W' nrs='0.29 / W'
+ sa=0 sb=0 sd=0 mult=1 m=1
XM64 GND net9 net7 GND sky130_fd_pr__nfet_01v8 L=.6 W=1.5 nf=1 ad='int((nf+1)/2) * W/nf * 0.29' as='int((nf+2)/2) * W/nf * 0.29'
+ pd='2*int((nf+1)/2) * (W/nf + 0.29)' ps='2*int((nf+2)/2) * (W/nf + 0.29)' nrd='0.29 / W' nrs='0.29 / W'
+ sa=0 sb=0 sd=0 mult=1 m=1
XMD68 VOUT GND GND GND sky130_fd_pr__nfet_01v8 L=.6 W=1.5 nf=1 ad='int((nf+1)/2) * W/nf * 0.29' as='int((nf+2)/2) * W/nf * 0.29'
+ pd='2*int((nf+1)/2) * (W/nf + 0.29)' ps='2*int((nf+2)/2) * (W/nf + 0.29)' nrd='0.29 / W' nrs='0.29 / W'
+ sa=0 sb=0 sd=0 mult=1 m=1
XM69 GND net9 net6 GND sky130_fd_pr__nfet_01v8 L=.6 W=1.5 nf=1 ad='int((nf+1)/2) * W/nf * 0.29' as='int((nf+2)/2) * W/nf * 0.29'
+ pd='2*int((nf+1)/2) * (W/nf + 0.29)' ps='2*int((nf+2)/2) * (W/nf + 0.29)' nrd='0.29 / W' nrs='0.29 / W'
+ sa=0 sb=0 sd=0 mult=1 m=1
XM70 net7 net18 net18 GND sky130_fd_pr__nfet_01v8 L=.6 W=1.5 nf=1 ad='int((nf+1)/2) * W/nf * 0.29' as='int((nf+2)/2) * W/nf * 0.29'
+ pd='2*int((nf+1)/2) * (W/nf + 0.29)' ps='2*int((nf+2)/2) * (W/nf + 0.29)' nrd='0.29 / W' nrs='0.29 / W'
+ sa=0 sb=0 sd=0 mult=1 m=1
XM71 net6 net18 net2 GND sky130_fd_pr__nfet_01v8 L=.6 W=1.5 nf=1 ad='int((nf+1)/2) * W/nf * 0.29' as='int((nf+2)/2) * W/nf * 0.29'
+ pd='2*int((nf+1)/2) * (W/nf + 0.29)' ps='2*int((nf+2)/2) * (W/nf + 0.29)' nrd='0.29 / W' nrs='0.29 / W'
+ sa=0 sb=0 sd=0 mult=1 m=1
XMD72 VOUT GND GND GND sky130_fd_pr__nfet_01v8 L=.6 W=1.5 nf=1 ad='int((nf+1)/2) * W/nf * 0.29' as='int((nf+2)/2) * W/nf * 0.29'
+ pd='2*int((nf+1)/2) * (W/nf + 0.29)' ps='2*int((nf+2)/2) * (W/nf + 0.29)' nrd='0.29 / W' nrs='0.29 / W'
+ sa=0 sb=0 sd=0 mult=1 m=1
XM73 GND net2 VOUT GND sky130_fd_pr__nfet_01v8 L=.6 W=1.5 nf=1 ad='int((nf+1)/2) * W/nf * 0.29' as='int((nf+2)/2) * W/nf * 0.29'
+ pd='2*int((nf+1)/2) * (W/nf + 0.29)' ps='2*int((nf+2)/2) * (W/nf + 0.29)' nrd='0.29 / W' nrs='0.29 / W'
+ sa=0 sb=0 sd=0 mult=1 m=1
XM74 GND net2 VOUT GND sky130_fd_pr__nfet_01v8 L=.6 W=1.5 nf=1 ad='int((nf+1)/2) * W/nf * 0.29' as='int((nf+2)/2) * W/nf * 0.29'
+ pd='2*int((nf+1)/2) * (W/nf + 0.29)' ps='2*int((nf+2)/2) * (W/nf + 0.29)' nrd='0.29 / W' nrs='0.29 / W'
+ sa=0 sb=0 sd=0 mult=1 m=1
XM75 net21 net10 GND VDD sky130_fd_pr__pfet_01v8 L=.6 W=1.5 nf=1 ad='int((nf+1)/2) * W/nf * 0.29' as='int((nf+2)/2) * W/nf * 0.29'
+ pd='2*int((nf+1)/2) * (W/nf + 0.29)' ps='2*int((nf+2)/2) * (W/nf + 0.29)' nrd='0.29 / W' nrs='0.29 / W'
+ sa=0 sb=0 sd=0 mult=1 m=1
XM76 net10 net10 net4 VDD sky130_fd_pr__pfet_01v8 L=.6 W=1.5 nf=1 ad='int((nf+1)/2) * W/nf * 0.29' as='int((nf+2)/2) * W/nf * 0.29'
+ pd='2*int((nf+1)/2) * (W/nf + 0.29)' ps='2*int((nf+2)/2) * (W/nf + 0.29)' nrd='0.29 / W' nrs='0.29 / W'
+ sa=0 sb=0 sd=0 mult=1 m=1
XM77 net17 net9 VDD GND sky130_fd_pr__nfet_01v8 L=.6 W=1.5 nf=1 ad='int((nf+1)/2) * W/nf * 0.29' as='int((nf+2)/2) * W/nf * 0.29'
+ pd='2*int((nf+1)/2) * (W/nf + 0.29)' ps='2*int((nf+2)/2) * (W/nf + 0.29)' nrd='0.29 / W' nrs='0.29 / W'
+ sa=0 sb=0 sd=0 mult=1 m=1
XM78 net9 net9 net7 GND sky130_fd_pr__nfet_01v8 L=.6 W=1.5 nf=1 ad='int((nf+1)/2) * W/nf * 0.29' as='int((nf+2)/2) * W/nf * 0.29'
+ pd='2*int((nf+1)/2) * (W/nf + 0.29)' ps='2*int((nf+2)/2) * (W/nf + 0.29)' nrd='0.29 / W' nrs='0.29 / W'
+ sa=0 sb=0 sd=0 mult=1 m=1
XMD79 VDD GND GND GND sky130_fd_pr__nfet_01v8 L=.6 W=1.5 nf=1 ad='int((nf+1)/2) * W/nf * 0.29' as='int((nf+2)/2) * W/nf * 0.29'
+ pd='2*int((nf+1)/2) * (W/nf + 0.29)' ps='2*int((nf+2)/2) * (W/nf + 0.29)' nrd='0.29 / W' nrs='0.29 / W'
+ sa=0 sb=0 sd=0 mult=1 m=1
XMD80 net7 GND GND GND sky130_fd_pr__nfet_01v8 L=.6 W=1.5 nf=1 ad='int((nf+1)/2) * W/nf * 0.29' as='int((nf+2)/2) * W/nf * 0.29'
+ pd='2*int((nf+1)/2) * (W/nf + 0.29)' ps='2*int((nf+2)/2) * (W/nf + 0.29)' nrd='0.29 / W' nrs='0.29 / W'
+ sa=0 sb=0 sd=0 mult=1 m=1
XMD81 GND VDD VDD VDD sky130_fd_pr__pfet_01v8 L=.6 W=1.5 nf=1 ad='int((nf+1)/2) * W/nf * 0.29' as='int((nf+2)/2) * W/nf * 0.29'
+ pd='2*int((nf+1)/2) * (W/nf + 0.29)' ps='2*int((nf+2)/2) * (W/nf + 0.29)' nrd='0.29 / W' nrs='0.29 / W'
+ sa=0 sb=0 sd=0 mult=1 m=1
XMD82 net4 VDD VDD VDD sky130_fd_pr__pfet_01v8 L=.6 W=1.5 nf=1 ad='int((nf+1)/2) * W/nf * 0.29' as='int((nf+2)/2) * W/nf * 0.29'
+ pd='2*int((nf+1)/2) * (W/nf + 0.29)' ps='2*int((nf+2)/2) * (W/nf + 0.29)' nrd='0.29 / W' nrs='0.29 / W'
+ sa=0 sb=0 sd=0 mult=1 m=1
XMD83 net24 GND net3 GND sky130_fd_pr__nfet_01v8 L=.6 W=1.5 nf=1 ad='int((nf+1)/2) * W/nf * 0.29' as='int((nf+2)/2) * W/nf * 0.29'
+ pd='2*int((nf+1)/2) * (W/nf + 0.29)' ps='2*int((nf+2)/2) * (W/nf + 0.29)' nrd='0.29 / W' nrs='0.29 / W'
+ sa=0 sb=0 sd=0 mult=1 m=1
XMD84 net25 GND net4 GND sky130_fd_pr__nfet_01v8 L=.6 W=1.5 nf=1 ad='int((nf+1)/2) * W/nf * 0.29' as='int((nf+2)/2) * W/nf * 0.29'
+ pd='2*int((nf+1)/2) * (W/nf + 0.29)' ps='2*int((nf+2)/2) * (W/nf + 0.29)' nrd='0.29 / W' nrs='0.29 / W'
+ sa=0 sb=0 sd=0 mult=1 m=1
XMD85 net22 VDD net6 VDD sky130_fd_pr__pfet_01v8 L=.6 W=1.5 nf=1 ad='int((nf+1)/2) * W/nf * 0.29' as='int((nf+2)/2) * W/nf * 0.29'
+ pd='2*int((nf+1)/2) * (W/nf + 0.29)' ps='2*int((nf+2)/2) * (W/nf + 0.29)' nrd='0.29 / W' nrs='0.29 / W'
+ sa=0 sb=0 sd=0 mult=1 m=1
XMD86 net23 VDD net7 VDD sky130_fd_pr__pfet_01v8 L=.6 W=1.5 nf=1 ad='int((nf+1)/2) * W/nf * 0.29' as='int((nf+2)/2) * W/nf * 0.29'
+ pd='2*int((nf+1)/2) * (W/nf + 0.29)' ps='2*int((nf+2)/2) * (W/nf + 0.29)' nrd='0.29 / W' nrs='0.29 / W'
+ sa=0 sb=0 sd=0 mult=1 m=1
XC1 net2 VOUT sky130_fd_pr__cap_mim_m3_1 W=20 L=12 MF=1 m=1
.ends


* expanding   symbol:  srlatch.sym # of pins=7
** sym_path: schematics/srlatch.sym
** sch_path: schematics/srlatch.sch
.subckt srlatch Enable S R VP VN Qb Q
*.ipin S
*.ipin R
*.iopin VP
*.iopin VN
*.opin Q
*.opin Qb
*.ipin Enable
X1 net1 Q VP VN Qb nor
X2 Qb net2 VP VN Q nor
X3 S Enable VP VN net1 and
X4 Enable R VP VN net2 and
.ends


* expanding   symbol:  /home/madvlsi/Documents/MADVLSI_final/schematics/current_boost.sym # of
*+ pins=2
** sym_path: schematics/current_boost.sym
** sch_path: schematics/current_boost.sch
.subckt current_boost Vsense VIboost
*.ipin Vsense
*.opin VIboost
XR1 net1 VIboost GND sky130_fd_pr__res_xhigh_po_0p35 L=43.75 mult=1 m=1
XR2 GND net1 GND sky130_fd_pr__res_xhigh_po_0p35 L=1.65 mult=1 m=1
X1 Vsense net1 VIboost opamp
.ends


* expanding   symbol:  /home/madvlsi/Documents/MADVLSI_final/schematics/error_amp.sym # of pins=4
** sym_path: schematics/error_amp.sym
** sch_path: schematics/error_amp.sch
.subckt error_amp Vref Cap1 Vfb Cap2
*.ipin Vfb
*.ipin Vref
*.iopin Cap1
*.iopin Cap2
XR1 Cap1 Vfb GND sky130_fd_pr__res_xhigh_po_0p35 L=8.65 mult=1 m=1
X1 Vref Vfb Cap2 opamp
.ends


* expanding   symbol:  /home/madvlsi/Documents/MADVLSI_final/schematics/PI_controller.sym # of
*+ pins=6
** sym_path: schematics/PI_controller.sym
** sch_path: schematics/PI_controller.sch
.subckt PI_controller Vref Cap1 Verror Cap2 Vint Vprop
*.ipin Verror
*.ipin Vref
*.iopin Cap1
*.iopin Cap2
*.opin Vint
*.opin Vprop
XR1 net1 net2 GND sky130_fd_pr__res_xhigh_po_0p35 L=1.65 mult=1 m=1
XR2 Vref net1 GND sky130_fd_pr__res_xhigh_po_0p35 L=1.65 mult=1 m=1
XR3 Verror Cap1 GND sky130_fd_pr__res_xhigh_po_0p35 L=1.65 mult=1 m=1
XR4 Cap1 Cap2 GND sky130_fd_pr__res_xhigh_po_0p35 L=8.65 mult=1 m=1
XR5 Cap2 net3 GND sky130_fd_pr__res_xhigh_po_0p35 L=1.65 mult=1 m=1
XR6 net3 Vint GND sky130_fd_pr__res_xhigh_po_0p35 L=8.65 mult=1 m=1
X1 Vref Cap1 Cap2 opamp
X2 Vref net3 Vint opamp
X3 net1 Vprop Vprop opamp
X4 Verror net2 net2 opamp
.ends


* expanding   symbol:  /home/madvlsi/Documents/MADVLSI_final/schematics/summing_amp.sym # of pins=4
** sym_path: schematics/summing_amp.sym
** sch_path: schematics/summing_amp.sch
.subckt summing_amp Vref Vpi Vint Vprop
*.ipin Vref
*.ipin Vint
*.ipin Vprop
*.opin Vpi
XR3 net1 Vint GND sky130_fd_pr__res_xhigh_po_0p35 L=1.65 mult=1 m=1
XR5 Vprop net1 GND sky130_fd_pr__res_xhigh_po_0p35 L=1.65 mult=1 m=1
XR1 net2 Vpi GND sky130_fd_pr__res_xhigh_po_0p35 L=1.65 mult=1 m=1
XR2 Vref net2 GND sky130_fd_pr__res_xhigh_po_0p35 L=1.65 mult=1 m=1
X1 net1 net2 Vpi opamp
.ends


* expanding   symbol:  /home/madvlsi/Documents/MADVLSI_final/schematics/nor.sym # of pins=5
** sym_path: schematics/nor.sym
** sch_path: schematics/nor.sch
.subckt nor A B VP VN Z
*.ipin A
*.ipin B
*.iopin VP
*.iopin VN
*.opin Z
**** begin user architecture code

.param l=.15
.param w=1

**** end user architecture code
XM1 Z A VN GND sky130_fd_pr__nfet_01v8 L=l W=w nf=1 ad='int((nf+1)/2) * W/nf * 0.29' as='int((nf+2)/2) * W/nf * 0.29'
+ pd='2*int((nf+1)/2) * (W/nf + 0.29)' ps='2*int((nf+2)/2) * (W/nf + 0.29)' nrd='0.29 / W' nrs='0.29 / W'
+ sa=0 sb=0 sd=0 mult=1 m=1
XM2 VN B Z GND sky130_fd_pr__nfet_01v8 L=l W=w nf=1 ad='int((nf+1)/2) * W/nf * 0.29' as='int((nf+2)/2) * W/nf * 0.29'
+ pd='2*int((nf+1)/2) * (W/nf + 0.29)' ps='2*int((nf+2)/2) * (W/nf + 0.29)' nrd='0.29 / W' nrs='0.29 / W'
+ sa=0 sb=0 sd=0 mult=1 m=1
XM3 Z A net1 VDD sky130_fd_pr__pfet_01v8 L=l W=w nf=1 ad='int((nf+1)/2) * W/nf * 0.29' as='int((nf+2)/2) * W/nf * 0.29'
+ pd='2*int((nf+1)/2) * (W/nf + 0.29)' ps='2*int((nf+2)/2) * (W/nf + 0.29)' nrd='0.29 / W' nrs='0.29 / W'
+ sa=0 sb=0 sd=0 mult=1 m=1
XM4 VP B net1 VDD sky130_fd_pr__pfet_01v8 L=l W=w nf=1 ad='int((nf+1)/2) * W/nf * 0.29' as='int((nf+2)/2) * W/nf * 0.29'
+ pd='2*int((nf+1)/2) * (W/nf + 0.29)' ps='2*int((nf+2)/2) * (W/nf + 0.29)' nrd='0.29 / W' nrs='0.29 / W'
+ sa=0 sb=0 sd=0 mult=1 m=1
.ends


* expanding   symbol:  /home/madvlsi/Documents/MADVLSI_final/schematics/and.sym # of pins=6
** sym_path: schematics/and.sym
** sch_path: schematics/and.sch
.subckt and A B VP VN Z
*.ipin A
*.ipin B
*.iopin VP
*.iopin VN
*.opin Z
X1 net1 VP VN Z inverter
X2 A B VP VN net1 nand
**** begin user architecture code

.param l=.15
.param w=1
.param mn=1
.param mp=1

**** end user architecture code
.ends


* expanding   symbol:  /home/madvlsi/Documents/final/xschem/inverter.sym # of pins=4
** sym_path: schematics/inverter.sym
** sch_path: schematics/inverter.sch
.subckt inverter A VP VN Z
*.ipin A
*.iopin VP
*.iopin VN
*.opin Z
XM1 Z A VN GND sky130_fd_pr__nfet_01v8 L=0.15 W=1 nf=1 ad='int((nf+1)/2) * W/nf * 0.29' as='int((nf+2)/2) * W/nf * 0.29'
+ pd='2*int((nf+1)/2) * (W/nf + 0.29)' ps='2*int((nf+2)/2) * (W/nf + 0.29)' nrd='0.29 / W' nrs='0.29 / W'
+ sa=0 sb=0 sd=0 mult=1 m=1
XM2 Z A VP VDD sky130_fd_pr__pfet_01v8 L=0.15 W=1 nf=1 ad='int((nf+1)/2) * W/nf * 0.29' as='int((nf+2)/2) * W/nf * 0.29'
+ pd='2*int((nf+1)/2) * (W/nf + 0.29)' ps='2*int((nf+2)/2) * (W/nf + 0.29)' nrd='0.29 / W' nrs='0.29 / W'
+ sa=0 sb=0 sd=0 mult=2 m=2
**** begin user architecture code

.param l=.15
.param w=1
.param mn=1
.param mp=1

**** end user architecture code
.ends


* expanding   symbol:  /home/madvlsi/Documents/final/xschem/nand.sym # of pins=6
** sym_path: schematics/nand.sym
** sch_path: schematics/nand.sch
.subckt nand A B VP VN Z
*.ipin A
*.iopin VP
*.iopin VN
*.opin Z
*.ipin B
XM1 Z A net1 GND sky130_fd_pr__nfet_01v8 L=0.15 W=1 nf=1 ad='int((nf+1)/2) * W/nf * 0.29' as='int((nf+2)/2) * W/nf * 0.29'
+ pd='2*int((nf+1)/2) * (W/nf + 0.29)' ps='2*int((nf+2)/2) * (W/nf + 0.29)' nrd='0.29 / W' nrs='0.29 / W'
+ sa=0 sb=0 sd=0 mult=1 m=1
XM2 VP B Z VDD sky130_fd_pr__pfet_01v8 L=0.15 W=1 nf=1 ad='int((nf+1)/2) * W/nf * 0.29' as='int((nf+2)/2) * W/nf * 0.29'
+ pd='2*int((nf+1)/2) * (W/nf + 0.29)' ps='2*int((nf+2)/2) * (W/nf + 0.29)' nrd='0.29 / W' nrs='0.29 / W'
+ sa=0 sb=0 sd=0 mult=2 m=2
XM3 VN B net1 GND sky130_fd_pr__nfet_01v8 L=0.15 W=1 nf=1 ad='int((nf+1)/2) * W/nf * 0.29' as='int((nf+2)/2) * W/nf * 0.29'
+ pd='2*int((nf+1)/2) * (W/nf + 0.29)' ps='2*int((nf+2)/2) * (W/nf + 0.29)' nrd='0.29 / W' nrs='0.29 / W'
+ sa=0 sb=0 sd=0 mult=1 m=1
XM4 Z A VP VDD sky130_fd_pr__pfet_01v8 L=0.15 W=1 nf=1 ad='int((nf+1)/2) * W/nf * 0.29' as='int((nf+2)/2) * W/nf * 0.29'
+ pd='2*int((nf+1)/2) * (W/nf + 0.29)' ps='2*int((nf+2)/2) * (W/nf + 0.29)' nrd='0.29 / W' nrs='0.29 / W'
+ sa=0 sb=0 sd=0 mult=2 m=2
.ends

.GLOBAL GND
.GLOBAL VDD
.end
